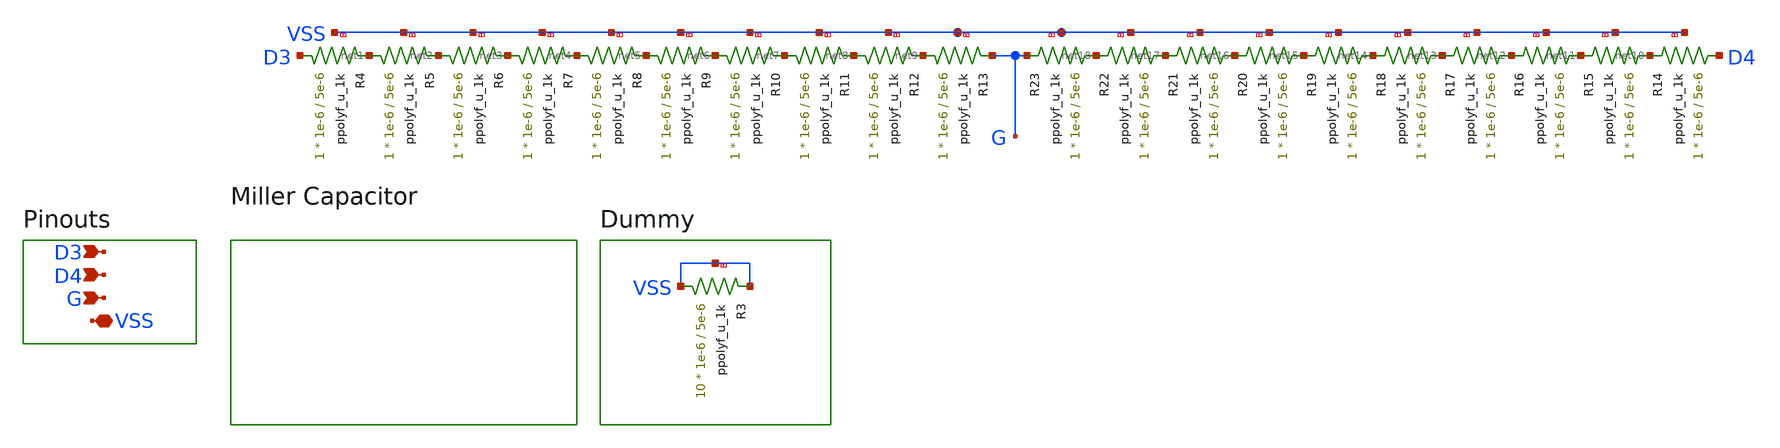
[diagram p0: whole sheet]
** sch_path: designs/libs/core_ota/differential_load_res/differential_load_res.sch
**.subckt differential_load_res VSS D3 D4 G
*.iopin VSS
*.ipin D3
*.ipin D4
*.ipin G
XR3 VSS VSS VSS ppolyf_u_1k r_width=1e-6 r_length=5e-6 m=10
XR4 D3 net1 VSS ppolyf_u_1k r_width=1e-6 r_length=5e-6 m=1
XR5 net1 net2 VSS ppolyf_u_1k r_width=1e-6 r_length=5e-6 m=1
XR6 net2 net3 VSS ppolyf_u_1k r_width=1e-6 r_length=5e-6 m=1
XR7 net3 net4 VSS ppolyf_u_1k r_width=1e-6 r_length=5e-6 m=1
XR8 net4 net5 VSS ppolyf_u_1k r_width=1e-6 r_length=5e-6 m=1
XR9 net5 net6 VSS ppolyf_u_1k r_width=1e-6 r_length=5e-6 m=1
XR10 net6 net7 VSS ppolyf_u_1k r_width=1e-6 r_length=5e-6 m=1
XR11 net7 net8 VSS ppolyf_u_1k r_width=1e-6 r_length=5e-6 m=1
XR12 net8 net9 VSS ppolyf_u_1k r_width=1e-6 r_length=5e-6 m=1
XR13 net9 G VSS ppolyf_u_1k r_width=1e-6 r_length=5e-6 m=1
XR14 D4 net10 VSS ppolyf_u_1k r_width=1e-6 r_length=5e-6 m=1
XR15 net10 net11 VSS ppolyf_u_1k r_width=1e-6 r_length=5e-6 m=1
XR16 net11 net12 VSS ppolyf_u_1k r_width=1e-6 r_length=5e-6 m=1
XR17 net12 net13 VSS ppolyf_u_1k r_width=1e-6 r_length=5e-6 m=1
XR18 net13 net14 VSS ppolyf_u_1k r_width=1e-6 r_length=5e-6 m=1
XR19 net14 net15 VSS ppolyf_u_1k r_width=1e-6 r_length=5e-6 m=1
XR20 net15 net16 VSS ppolyf_u_1k r_width=1e-6 r_length=5e-6 m=1
XR21 net16 net17 VSS ppolyf_u_1k r_width=1e-6 r_length=5e-6 m=1
XR22 net17 net18 VSS ppolyf_u_1k r_width=1e-6 r_length=5e-6 m=1
XR23 net18 G VSS ppolyf_u_1k r_width=1e-6 r_length=5e-6 m=1
**.ends
.end
